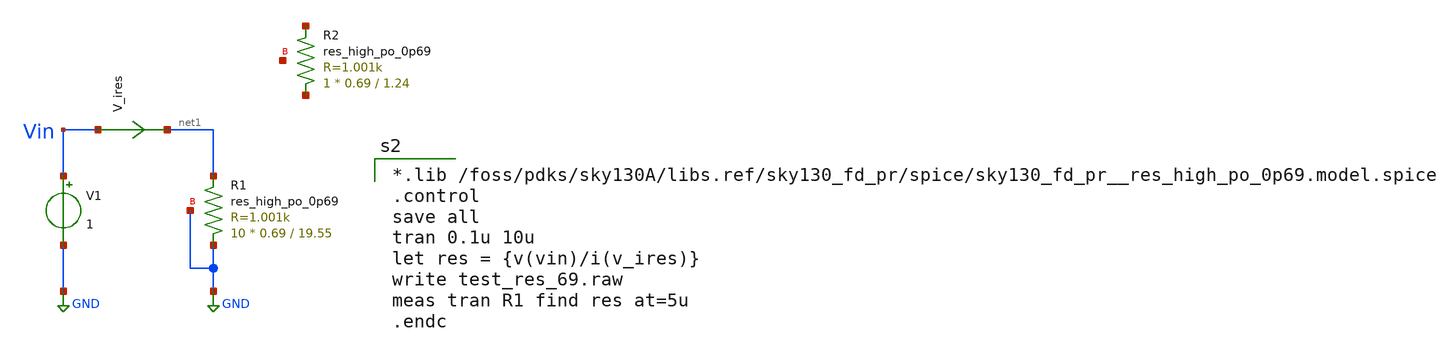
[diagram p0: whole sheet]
** sch_path: test_res_69.sch
**.subckt test_res_69
V1 Vin GND 1
V_ires Vin net1 0
.save i(v_ires)
XR1 GND net1 GND sky130_fd_pr__res_high_po_0p69 L=19.55 mult=10 m=10
XR2 net2 net3 net4 sky130_fd_pr__res_high_po_0p69 L=1.24 mult=1 m=1
**** begin user architecture code

*.lib /foss/pdks/sky130A/libs.ref/sky130_fd_pr/spice/sky130_fd_pr__res_high_po_0p69.model.spice
.control
save all
tran 0.1u 10u
let res = {v(vin)/i(v_ires)}
write test_res_69.raw
meas tran R1 find res at=5u
.endc


** opencircuitdesign pdks install
.lib $::SKYWATER_MODELS/sky130.lib.spice tt


**** end user architecture code
**.ends
.GLOBAL GND
.end
